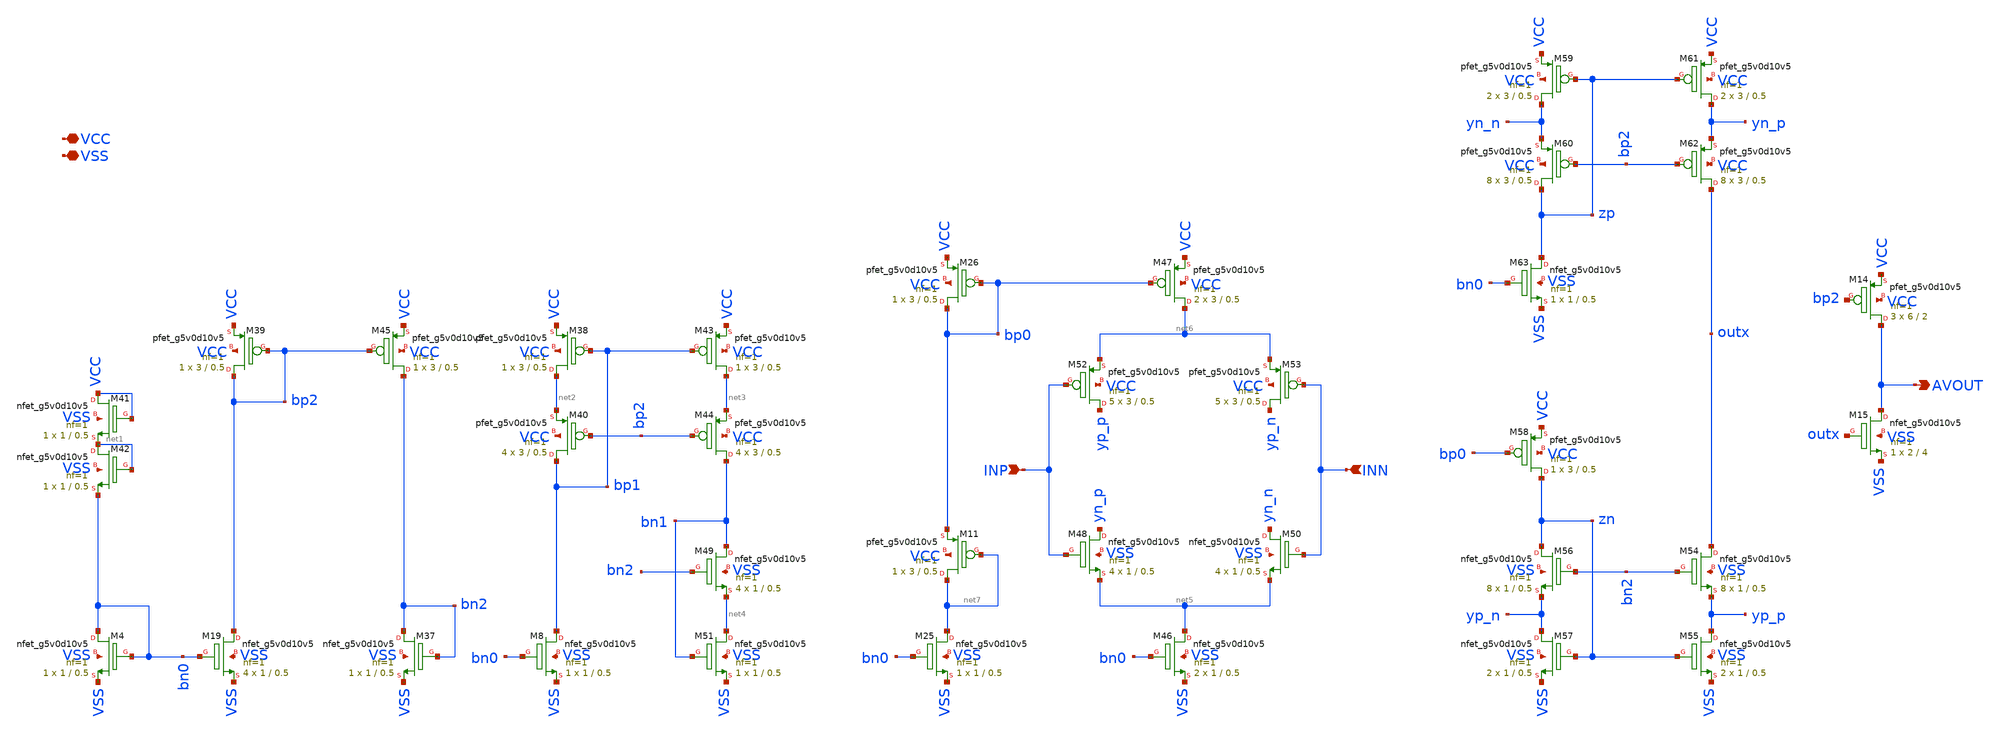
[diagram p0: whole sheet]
** sch_path: folded_cascode/LUIS/folded_cascode.sch
**.subckt folded_cascode VCC VSS INN INP AVOUT
*.iopin VCC
*.iopin VSS
*.ipin INN
*.ipin INP
*.opin AVOUT
XM41 VCC VCC net1 VSS sky130_fd_pr__nfet_g5v0d10v5 L=0.5 W=1 nf=1 ad='int((nf+1)/2) * W/nf * 0.29' as='int((nf+2)/2) * W/nf * 0.29'
+ pd='2*int((nf+1)/2) * (W/nf + 0.29)' ps='2*int((nf+2)/2) * (W/nf + 0.29)' nrd='0.29 / W' nrs='0.29 / W'
+ sa=0 sb=0 sd=0 mult=1 m=1
XM42 net1 net1 bn0 VSS sky130_fd_pr__nfet_g5v0d10v5 L=0.5 W=1 nf=1 ad='int((nf+1)/2) * W/nf * 0.29' as='int((nf+2)/2) * W/nf * 0.29'
+ pd='2*int((nf+1)/2) * (W/nf + 0.29)' ps='2*int((nf+2)/2) * (W/nf + 0.29)' nrd='0.29 / W' nrs='0.29 / W'
+ sa=0 sb=0 sd=0 mult=1 m=1
XM8 bp1 bn0 VSS VSS sky130_fd_pr__nfet_g5v0d10v5 L=0.5 W=1 nf=1 ad='int((nf+1)/2) * W/nf * 0.29' as='int((nf+2)/2) * W/nf * 0.29'
+ pd='2*int((nf+1)/2) * (W/nf + 0.29)' ps='2*int((nf+2)/2) * (W/nf + 0.29)' nrd='0.29 / W' nrs='0.29 / W'
+ sa=0 sb=0 sd=0 mult=1 m=1
XM38 net2 bp1 VCC VCC sky130_fd_pr__pfet_g5v0d10v5 L=0.5 W=3 nf=1 ad='int((nf+1)/2) * W/nf * 0.29' as='int((nf+2)/2) * W/nf * 0.29'
+ pd='2*int((nf+1)/2) * (W/nf + 0.29)' ps='2*int((nf+2)/2) * (W/nf + 0.29)' nrd='0.29 / W' nrs='0.29 / W'
+ sa=0 sb=0 sd=0 mult=1 m=1
XM40 bp1 bp2 net2 VCC sky130_fd_pr__pfet_g5v0d10v5 L=0.5 W=3 nf=1 ad='int((nf+1)/2) * W/nf * 0.29' as='int((nf+2)/2) * W/nf * 0.29'
+ pd='2*int((nf+1)/2) * (W/nf + 0.29)' ps='2*int((nf+2)/2) * (W/nf + 0.29)' nrd='0.29 / W' nrs='0.29 / W'
+ sa=0 sb=0 sd=0 mult=4 m=4
XM43 net3 bp1 VCC VCC sky130_fd_pr__pfet_g5v0d10v5 L=0.5 W=3 nf=1 ad='int((nf+1)/2) * W/nf * 0.29' as='int((nf+2)/2) * W/nf * 0.29'
+ pd='2*int((nf+1)/2) * (W/nf + 0.29)' ps='2*int((nf+2)/2) * (W/nf + 0.29)' nrd='0.29 / W' nrs='0.29 / W'
+ sa=0 sb=0 sd=0 mult=1 m=1
XM44 bn1 bp2 net3 VCC sky130_fd_pr__pfet_g5v0d10v5 L=0.5 W=3 nf=1 ad='int((nf+1)/2) * W/nf * 0.29' as='int((nf+2)/2) * W/nf * 0.29'
+ pd='2*int((nf+1)/2) * (W/nf + 0.29)' ps='2*int((nf+2)/2) * (W/nf + 0.29)' nrd='0.29 / W' nrs='0.29 / W'
+ sa=0 sb=0 sd=0 mult=4 m=4
XM49 bn1 bn2 net4 VSS sky130_fd_pr__nfet_g5v0d10v5 L=0.5 W=1 nf=1 ad='int((nf+1)/2) * W/nf * 0.29' as='int((nf+2)/2) * W/nf * 0.29'
+ pd='2*int((nf+1)/2) * (W/nf + 0.29)' ps='2*int((nf+2)/2) * (W/nf + 0.29)' nrd='0.29 / W' nrs='0.29 / W'
+ sa=0 sb=0 sd=0 mult=4 m=4
XM51 net4 bn1 VSS VSS sky130_fd_pr__nfet_g5v0d10v5 L=0.5 W=1 nf=1 ad='int((nf+1)/2) * W/nf * 0.29' as='int((nf+2)/2) * W/nf * 0.29'
+ pd='2*int((nf+1)/2) * (W/nf + 0.29)' ps='2*int((nf+2)/2) * (W/nf + 0.29)' nrd='0.29 / W' nrs='0.29 / W'
+ sa=0 sb=0 sd=0 mult=1 m=1
XM19 bp2 bn0 VSS VSS sky130_fd_pr__nfet_g5v0d10v5 L=0.5 W=1 nf=1 ad='int((nf+1)/2) * W/nf * 0.29' as='int((nf+2)/2) * W/nf * 0.29'
+ pd='2*int((nf+1)/2) * (W/nf + 0.29)' ps='2*int((nf+2)/2) * (W/nf + 0.29)' nrd='0.29 / W' nrs='0.29 / W'
+ sa=0 sb=0 sd=0 mult=4 m=4
XM37 bn2 bn2 VSS VSS sky130_fd_pr__nfet_g5v0d10v5 L=0.5 W=1 nf=1 ad='int((nf+1)/2) * W/nf * 0.29' as='int((nf+2)/2) * W/nf * 0.29'
+ pd='2*int((nf+1)/2) * (W/nf + 0.29)' ps='2*int((nf+2)/2) * (W/nf + 0.29)' nrd='0.29 / W' nrs='0.29 / W'
+ sa=0 sb=0 sd=0 mult=1 m=1
XM4 bn0 bn0 VSS VSS sky130_fd_pr__nfet_g5v0d10v5 L=0.5 W=1 nf=1 ad='int((nf+1)/2) * W/nf * 0.29' as='int((nf+2)/2) * W/nf * 0.29'
+ pd='2*int((nf+1)/2) * (W/nf + 0.29)' ps='2*int((nf+2)/2) * (W/nf + 0.29)' nrd='0.29 / W' nrs='0.29 / W'
+ sa=0 sb=0 sd=0 mult=1 m=1
XM39 bp2 bp2 VCC VCC sky130_fd_pr__pfet_g5v0d10v5 L=0.5 W=3 nf=1 ad='int((nf+1)/2) * W/nf * 0.29' as='int((nf+2)/2) * W/nf * 0.29'
+ pd='2*int((nf+1)/2) * (W/nf + 0.29)' ps='2*int((nf+2)/2) * (W/nf + 0.29)' nrd='0.29 / W' nrs='0.29 / W'
+ sa=0 sb=0 sd=0 mult=1 m=1
XM45 bn2 bp2 VCC VCC sky130_fd_pr__pfet_g5v0d10v5 L=0.5 W=3 nf=1 ad='int((nf+1)/2) * W/nf * 0.29' as='int((nf+2)/2) * W/nf * 0.29'
+ pd='2*int((nf+1)/2) * (W/nf + 0.29)' ps='2*int((nf+2)/2) * (W/nf + 0.29)' nrd='0.29 / W' nrs='0.29 / W'
+ sa=0 sb=0 sd=0 mult=1 m=1
XM25 net7 bn0 VSS VSS sky130_fd_pr__nfet_g5v0d10v5 L=0.5 W=1 nf=1 ad='int((nf+1)/2) * W/nf * 0.29' as='int((nf+2)/2) * W/nf * 0.29'
+ pd='2*int((nf+1)/2) * (W/nf + 0.29)' ps='2*int((nf+2)/2) * (W/nf + 0.29)' nrd='0.29 / W' nrs='0.29 / W'
+ sa=0 sb=0 sd=0 mult=1 m=1
XM26 bp0 bp0 VCC VCC sky130_fd_pr__pfet_g5v0d10v5 L=0.5 W=3 nf=1 ad='int((nf+1)/2) * W/nf * 0.29' as='int((nf+2)/2) * W/nf * 0.29'
+ pd='2*int((nf+1)/2) * (W/nf + 0.29)' ps='2*int((nf+2)/2) * (W/nf + 0.29)' nrd='0.29 / W' nrs='0.29 / W'
+ sa=0 sb=0 sd=0 mult=1 m=1
XM46 net5 bn0 VSS VSS sky130_fd_pr__nfet_g5v0d10v5 L=0.5 W=1 nf=1 ad='int((nf+1)/2) * W/nf * 0.29' as='int((nf+2)/2) * W/nf * 0.29'
+ pd='2*int((nf+1)/2) * (W/nf + 0.29)' ps='2*int((nf+2)/2) * (W/nf + 0.29)' nrd='0.29 / W' nrs='0.29 / W'
+ sa=0 sb=0 sd=0 mult=2 m=2
XM47 net6 bp0 VCC VCC sky130_fd_pr__pfet_g5v0d10v5 L=0.5 W=3 nf=1 ad='int((nf+1)/2) * W/nf * 0.29' as='int((nf+2)/2) * W/nf * 0.29'
+ pd='2*int((nf+1)/2) * (W/nf + 0.29)' ps='2*int((nf+2)/2) * (W/nf + 0.29)' nrd='0.29 / W' nrs='0.29 / W'
+ sa=0 sb=0 sd=0 mult=2 m=2
XM48 yn_p INP net5 VSS sky130_fd_pr__nfet_g5v0d10v5 L=0.5 W=1 nf=1 ad='int((nf+1)/2) * W/nf * 0.29' as='int((nf+2)/2) * W/nf * 0.29'
+ pd='2*int((nf+1)/2) * (W/nf + 0.29)' ps='2*int((nf+2)/2) * (W/nf + 0.29)' nrd='0.29 / W' nrs='0.29 / W'
+ sa=0 sb=0 sd=0 mult=4 m=4
XM50 yn_n INN net5 VSS sky130_fd_pr__nfet_g5v0d10v5 L=0.5 W=1 nf=1 ad='int((nf+1)/2) * W/nf * 0.29' as='int((nf+2)/2) * W/nf * 0.29'
+ pd='2*int((nf+1)/2) * (W/nf + 0.29)' ps='2*int((nf+2)/2) * (W/nf + 0.29)' nrd='0.29 / W' nrs='0.29 / W'
+ sa=0 sb=0 sd=0 mult=4 m=4
XM52 yp_p INP net6 VCC sky130_fd_pr__pfet_g5v0d10v5 L=0.5 W=3 nf=1 ad='int((nf+1)/2) * W/nf * 0.29' as='int((nf+2)/2) * W/nf * 0.29'
+ pd='2*int((nf+1)/2) * (W/nf + 0.29)' ps='2*int((nf+2)/2) * (W/nf + 0.29)' nrd='0.29 / W' nrs='0.29 / W'
+ sa=0 sb=0 sd=0 mult=5 m=5
XM53 yp_n INN net6 VCC sky130_fd_pr__pfet_g5v0d10v5 L=0.5 W=3 nf=1 ad='int((nf+1)/2) * W/nf * 0.29' as='int((nf+2)/2) * W/nf * 0.29'
+ pd='2*int((nf+1)/2) * (W/nf + 0.29)' ps='2*int((nf+2)/2) * (W/nf + 0.29)' nrd='0.29 / W' nrs='0.29 / W'
+ sa=0 sb=0 sd=0 mult=5 m=5
XM54 outx bn2 yp_p VSS sky130_fd_pr__nfet_g5v0d10v5 L=0.5 W=1 nf=1 ad='int((nf+1)/2) * W/nf * 0.29' as='int((nf+2)/2) * W/nf * 0.29'
+ pd='2*int((nf+1)/2) * (W/nf + 0.29)' ps='2*int((nf+2)/2) * (W/nf + 0.29)' nrd='0.29 / W' nrs='0.29 / W'
+ sa=0 sb=0 sd=0 mult=8 m=8
XM55 yp_p zn VSS VSS sky130_fd_pr__nfet_g5v0d10v5 L=0.5 W=1 nf=1 ad='int((nf+1)/2) * W/nf * 0.29' as='int((nf+2)/2) * W/nf * 0.29'
+ pd='2*int((nf+1)/2) * (W/nf + 0.29)' ps='2*int((nf+2)/2) * (W/nf + 0.29)' nrd='0.29 / W' nrs='0.29 / W'
+ sa=0 sb=0 sd=0 mult=2 m=2
XM56 zn bn2 yp_n VSS sky130_fd_pr__nfet_g5v0d10v5 L=0.5 W=1 nf=1 ad='int((nf+1)/2) * W/nf * 0.29' as='int((nf+2)/2) * W/nf * 0.29'
+ pd='2*int((nf+1)/2) * (W/nf + 0.29)' ps='2*int((nf+2)/2) * (W/nf + 0.29)' nrd='0.29 / W' nrs='0.29 / W'
+ sa=0 sb=0 sd=0 mult=8 m=8
XM57 yp_n zn VSS VSS sky130_fd_pr__nfet_g5v0d10v5 L=0.5 W=1 nf=1 ad='int((nf+1)/2) * W/nf * 0.29' as='int((nf+2)/2) * W/nf * 0.29'
+ pd='2*int((nf+1)/2) * (W/nf + 0.29)' ps='2*int((nf+2)/2) * (W/nf + 0.29)' nrd='0.29 / W' nrs='0.29 / W'
+ sa=0 sb=0 sd=0 mult=2 m=2
XM58 zn bp0 VCC VCC sky130_fd_pr__pfet_g5v0d10v5 L=0.5 W=3 nf=1 ad='int((nf+1)/2) * W/nf * 0.29' as='int((nf+2)/2) * W/nf * 0.29'
+ pd='2*int((nf+1)/2) * (W/nf + 0.29)' ps='2*int((nf+2)/2) * (W/nf + 0.29)' nrd='0.29 / W' nrs='0.29 / W'
+ sa=0 sb=0 sd=0 mult=1 m=1
XM59 yn_n zp VCC VCC sky130_fd_pr__pfet_g5v0d10v5 L=0.5 W=3 nf=1 ad='int((nf+1)/2) * W/nf * 0.29' as='int((nf+2)/2) * W/nf * 0.29'
+ pd='2*int((nf+1)/2) * (W/nf + 0.29)' ps='2*int((nf+2)/2) * (W/nf + 0.29)' nrd='0.29 / W' nrs='0.29 / W'
+ sa=0 sb=0 sd=0 mult=2 m=2
XM60 zp bp2 yn_n VCC sky130_fd_pr__pfet_g5v0d10v5 L=0.5 W=3 nf=1 ad='int((nf+1)/2) * W/nf * 0.29' as='int((nf+2)/2) * W/nf * 0.29'
+ pd='2*int((nf+1)/2) * (W/nf + 0.29)' ps='2*int((nf+2)/2) * (W/nf + 0.29)' nrd='0.29 / W' nrs='0.29 / W'
+ sa=0 sb=0 sd=0 mult=8 m=8
XM61 yn_p zp VCC VCC sky130_fd_pr__pfet_g5v0d10v5 L=0.5 W=3 nf=1 ad='int((nf+1)/2) * W/nf * 0.29' as='int((nf+2)/2) * W/nf * 0.29'
+ pd='2*int((nf+1)/2) * (W/nf + 0.29)' ps='2*int((nf+2)/2) * (W/nf + 0.29)' nrd='0.29 / W' nrs='0.29 / W'
+ sa=0 sb=0 sd=0 mult=2 m=2
XM62 outx bp2 yn_p VCC sky130_fd_pr__pfet_g5v0d10v5 L=0.5 W=3 nf=1 ad='int((nf+1)/2) * W/nf * 0.29' as='int((nf+2)/2) * W/nf * 0.29'
+ pd='2*int((nf+1)/2) * (W/nf + 0.29)' ps='2*int((nf+2)/2) * (W/nf + 0.29)' nrd='0.29 / W' nrs='0.29 / W'
+ sa=0 sb=0 sd=0 mult=8 m=8
XM63 zp bn0 VSS VSS sky130_fd_pr__nfet_g5v0d10v5 L=0.5 W=1 nf=1 ad='int((nf+1)/2) * W/nf * 0.29' as='int((nf+2)/2) * W/nf * 0.29'
+ pd='2*int((nf+1)/2) * (W/nf + 0.29)' ps='2*int((nf+2)/2) * (W/nf + 0.29)' nrd='0.29 / W' nrs='0.29 / W'
+ sa=0 sb=0 sd=0 mult=1 m=1
XM11 net7 net7 bp0 VCC sky130_fd_pr__pfet_g5v0d10v5 L=0.5 W=3 nf=1 ad='int((nf+1)/2) * W/nf * 0.29' as='int((nf+2)/2) * W/nf * 0.29'
+ pd='2*int((nf+1)/2) * (W/nf + 0.29)' ps='2*int((nf+2)/2) * (W/nf + 0.29)' nrd='0.29 / W' nrs='0.29 / W'
+ sa=0 sb=0 sd=0 mult=1 m=1
XM15 AVOUT outx VSS VSS sky130_fd_pr__nfet_g5v0d10v5 L=4 W=2 nf=1 ad='int((nf+1)/2) * W/nf * 0.29' as='int((nf+2)/2) * W/nf * 0.29'
+ pd='2*int((nf+1)/2) * (W/nf + 0.29)' ps='2*int((nf+2)/2) * (W/nf + 0.29)' nrd='0.29 / W' nrs='0.29 / W'
+ sa=0 sb=0 sd=0 mult=1 m=1
XM14 AVOUT bp2 VCC VCC sky130_fd_pr__pfet_g5v0d10v5 L=2 W=6 nf=1 ad='int((nf+1)/2) * W/nf * 0.29' as='int((nf+2)/2) * W/nf * 0.29'
+ pd='2*int((nf+1)/2) * (W/nf + 0.29)' ps='2*int((nf+2)/2) * (W/nf + 0.29)' nrd='0.29 / W' nrs='0.29 / W'
+ sa=0 sb=0 sd=0 mult=3 m=3
**.ends
.end
